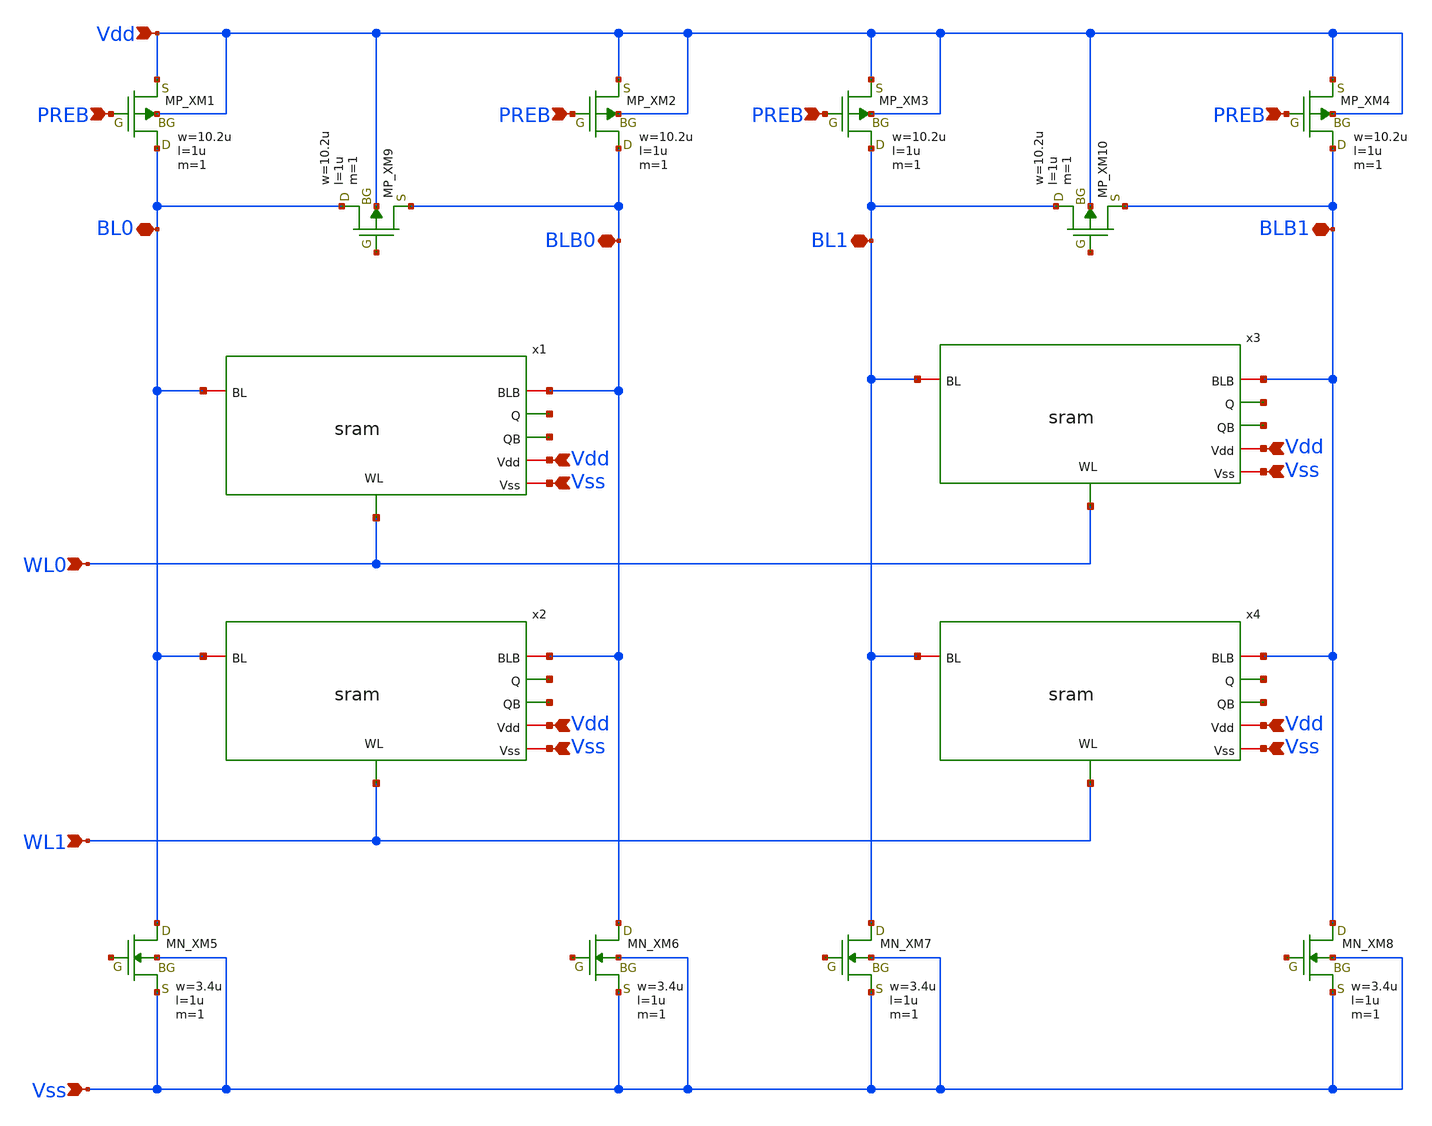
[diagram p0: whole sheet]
** sch_path: member_project/SRAM/PenguinEino/learning/schematics/sram_array.sch
**.subckt sram_array BL0 BLB0 BL1 BLB1 WL1 WL0 Vss Vdd Vss Vdd Vss Vdd Vss Vdd Vdd PREB PREB PREB
*+ PREB Vss
*.iopin BL0
*.iopin BLB0
*.iopin BL1
*.iopin BLB1
*.ipin WL1
*.ipin WL0
*.ipin Vss
*.ipin Vdd
*.ipin Vss
*.ipin Vdd
*.ipin Vss
*.ipin Vdd
*.ipin Vss
*.ipin Vdd
*.ipin Vdd
*.ipin PREB
*.ipin PREB
*.ipin PREB
*.ipin PREB
*.ipin Vss
x1 WL0 Vdd BLB0 net1 net2 BL0 Vss sram
x2 WL1 Vdd BLB0 net3 net4 BL0 Vss sram
x3 WL0 Vdd BLB1 net5 net6 BL1 Vss sram
x4 WL1 Vdd BLB1 net7 net8 BL1 Vss sram
XXM1 BL0 PREB Vdd Vdd PMOS w=10.2u l=1u nrd=0 nrs=0 m=1
XXM2 BLB0 PREB Vdd Vdd PMOS w=10.2u l=1u nrd=0 nrs=0 m=1
XXM3 BL1 PREB Vdd Vdd PMOS w=10.2u l=1u nrd=0 nrs=0 m=1
XXM4 BLB1 PREB Vdd Vdd PMOS w=10.2u l=1u nrd=0 nrs=0 m=1
XXM5 BL0 net9 Vss Vss NMOS w=3.4u l=1u nrd=0 nrs=0 m=1
XXM6 BLB0 net10 Vss Vss NMOS w=3.4u l=1u nrd=0 nrs=0 m=1
XXM7 BL1 net11 Vss Vss NMOS w=3.4u l=1u nrd=0 nrs=0 m=1
XXM8 BLB1 net12 Vss Vss NMOS w=3.4u l=1u nrd=0 nrs=0 m=1
XXM9 BL0 net13 BLB0 Vdd PMOS w=10.2u l=1u nrd=0 nrs=0 m=1
XXM10 BL1 net14 BLB1 Vdd PMOS w=10.2u l=1u nrd=0 nrs=0 m=1
**.ends
.end
